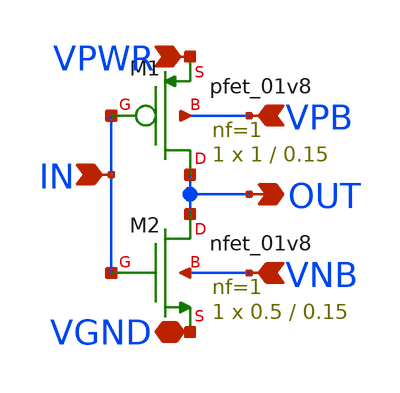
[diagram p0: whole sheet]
** sch_path: xschem/inv_bsw.sch
**.subckt inv_bsw IN OUT VPWR VPB VGND VNB
*.ipin IN
*.opin OUT
*.ipin VPWR
*.ipin VPB
*.iopin VGND
*.ipin VNB
XM2 OUT IN VGND VNB sky130_fd_pr__nfet_01v8 L=0.15 W=0.5 nf=1 ad='int((nf+1)/2) * W/nf * 0.29' as='int((nf+2)/2) * W/nf * 0.29'
+ pd='2*int((nf+1)/2) * (W/nf + 0.29)' ps='2*int((nf+2)/2) * (W/nf + 0.29)' nrd='0.29 / W' nrs='0.29 / W'
+ sa=0 sb=0 sd=0 mult=1 m=1
XM1 OUT IN VPWR VPB sky130_fd_pr__pfet_01v8 L=0.15 W=1 nf=1 ad='int((nf+1)/2) * W/nf * 0.29' as='int((nf+2)/2) * W/nf * 0.29'
+ pd='2*int((nf+1)/2) * (W/nf + 0.29)' ps='2*int((nf+2)/2) * (W/nf + 0.29)' nrd='0.29 / W' nrs='0.29 / W'
+ sa=0 sb=0 sd=0 mult=1 m=1
**.ends
.end
